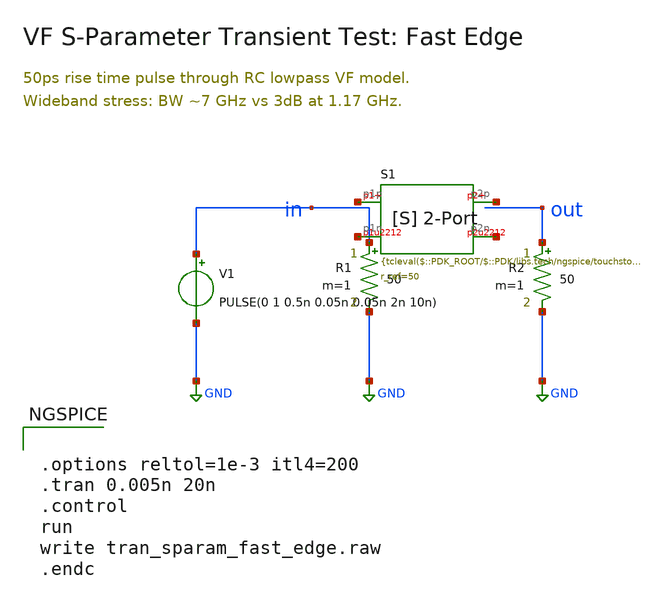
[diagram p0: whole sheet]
** sch_path: ihp-sg13g2/libs.tech/xschem/sg13g2_tests/tran_sparam_fast_edge.sch
* Copyright 2024 IHP PDK Authors
**.subckt tran_sparam_fast_edge
V1 in GND PULSE(0 1 0.5n 0.05n 0.05n 2n 10n)
R1 in GND 50 m=1
R2 out GND 50 m=1
AS1 [ net1 net2 net3 net4 ] lowpass_fast
.model lowpass_fast sparam( file=" r_ref=50 n_poles=0 vf_tol=1e-3 vf_maxiter=10 )
**** begin user architecture code


.options reltol=1e-3 itl4=200
.tran 0.005n 20n
.control
run
write tran_sparam_fast_edge.raw
.endc


**** end user architecture code
**.ends
.GLOBAL GND
.end
